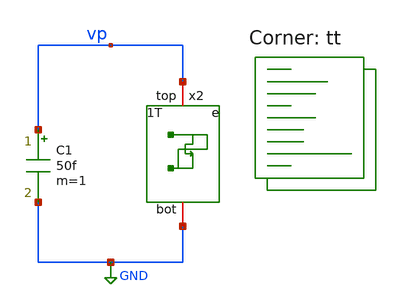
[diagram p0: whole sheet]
** sch_path: xschem/tb/dschr_nwk_1t_type_e_tb.sch
**.subckt dschr_nwk_1t_type_e_tb
C1 vp GND 50f m=1
x2 vp GND dschr_nwk_1t_type_e L=0.15 W=0.5
**** begin user architecture code
.lib $::SKYWATER_MODELS/sky130.lib.spice tt


.include $::netlist_dir/ctrl_sims.spice


**** end user architecture code
**.ends
.GLOBAL GND
.end
